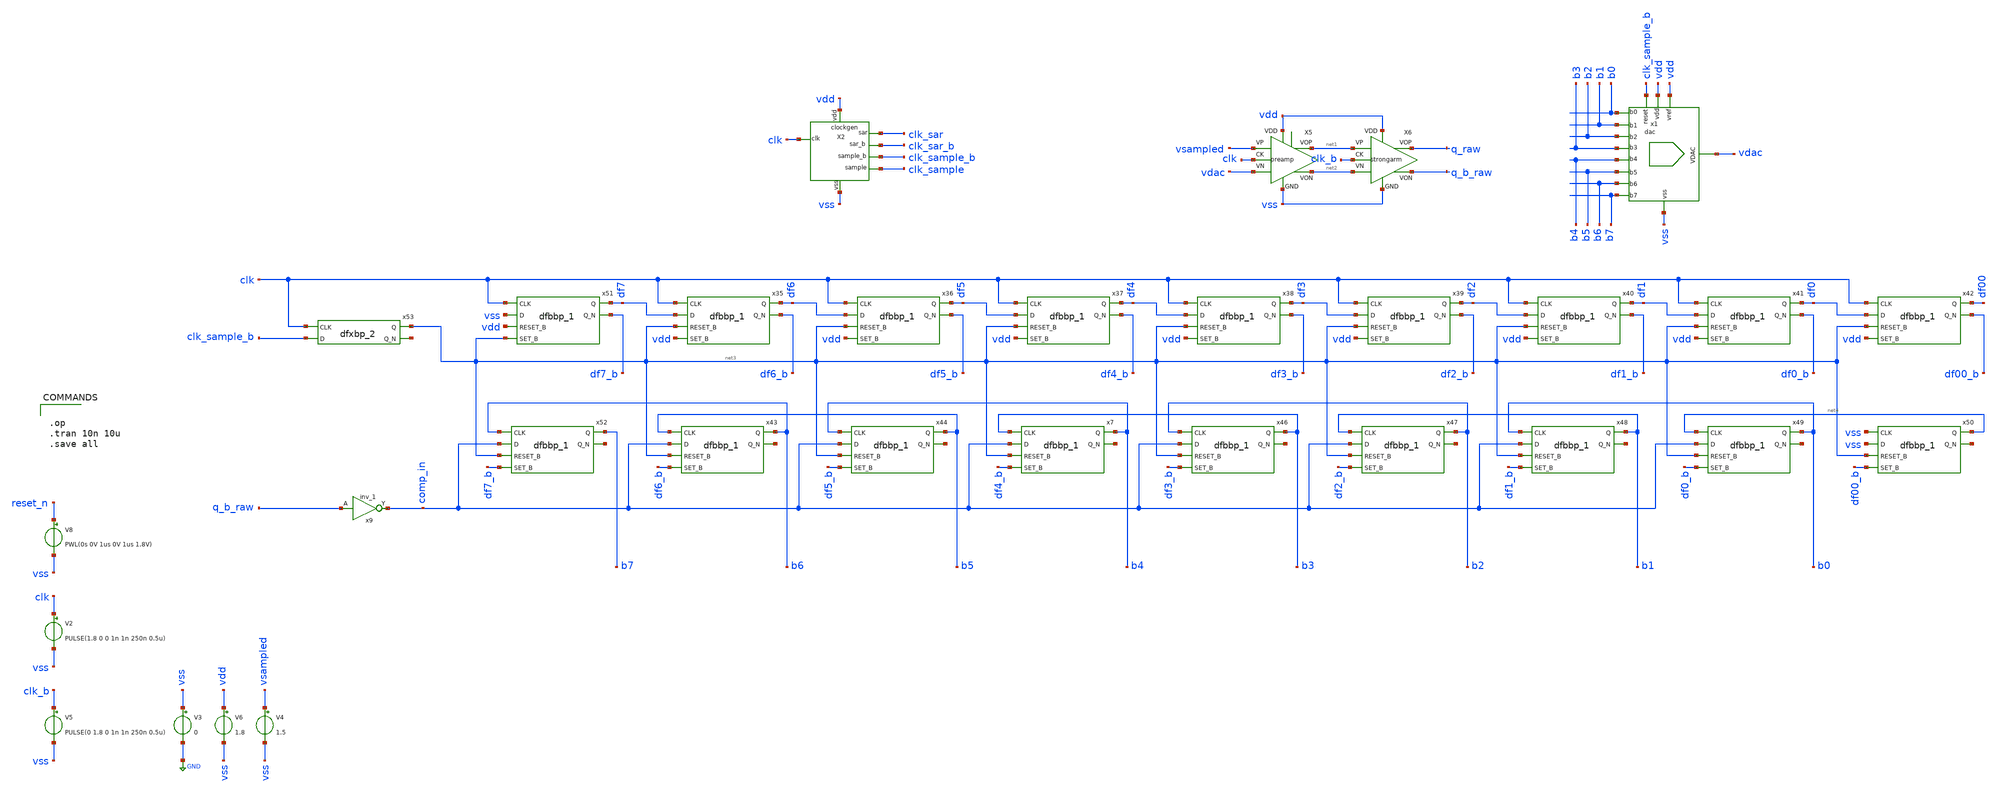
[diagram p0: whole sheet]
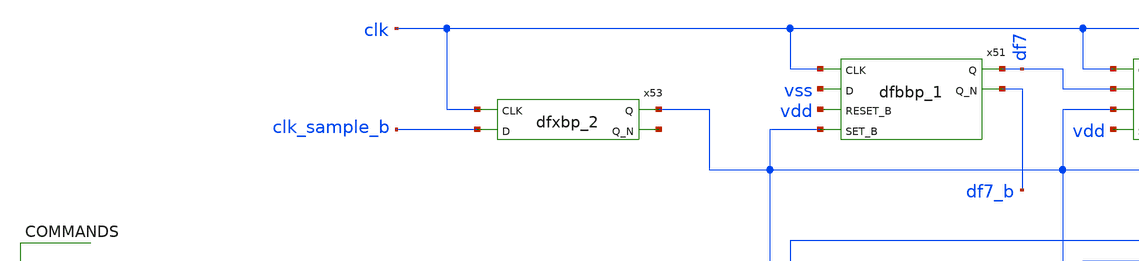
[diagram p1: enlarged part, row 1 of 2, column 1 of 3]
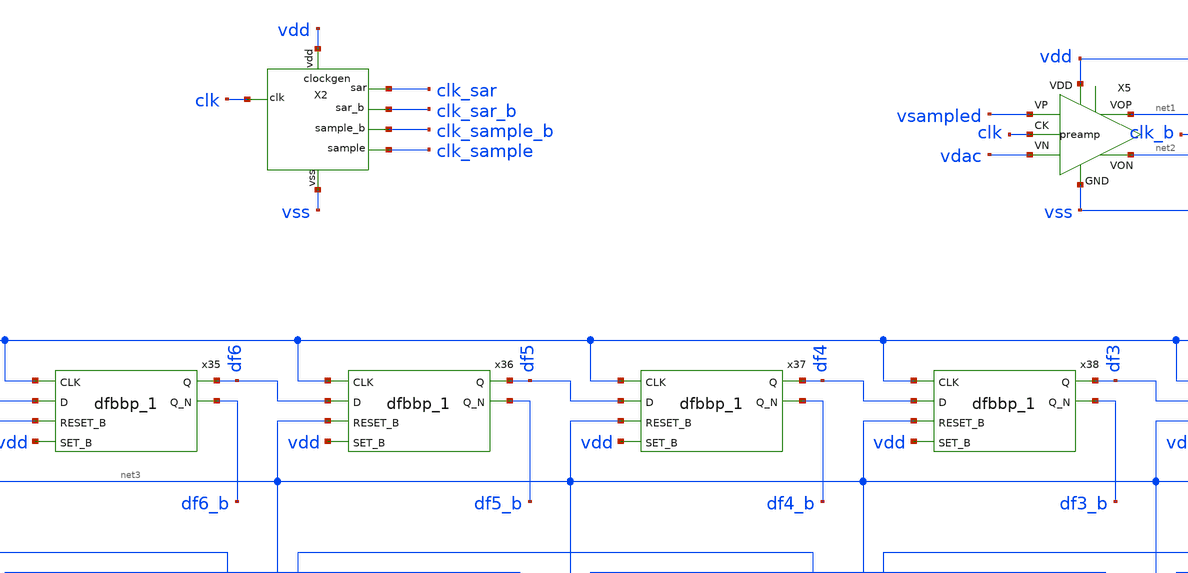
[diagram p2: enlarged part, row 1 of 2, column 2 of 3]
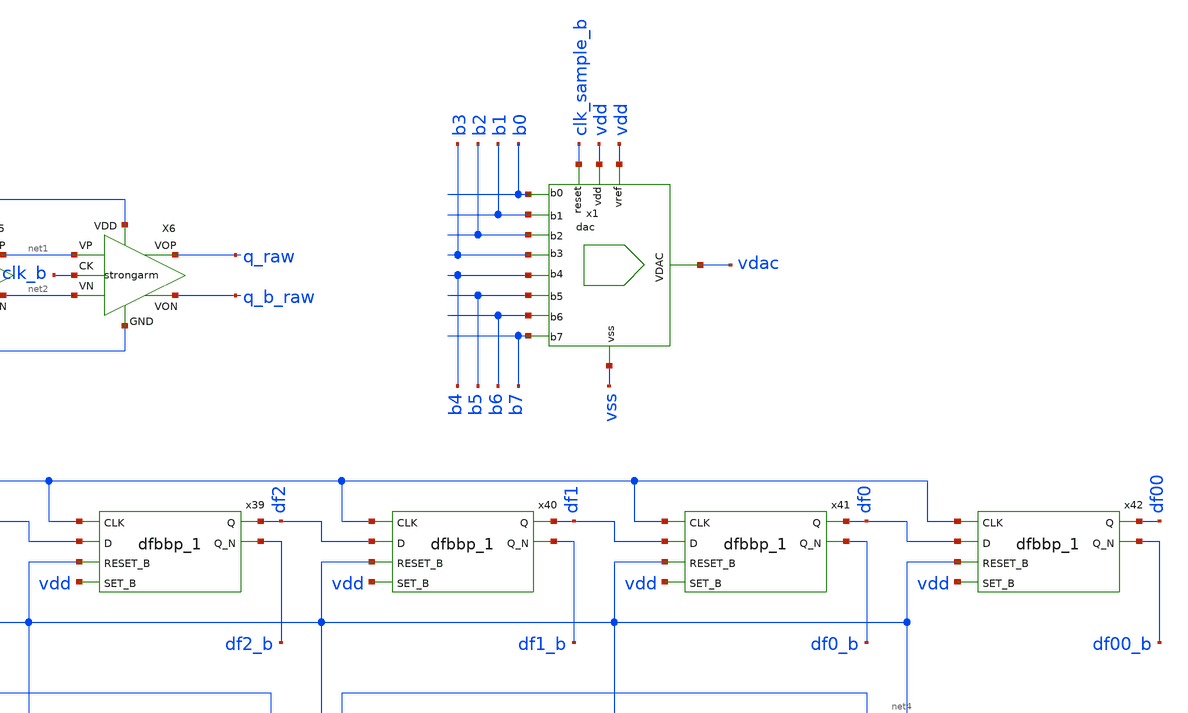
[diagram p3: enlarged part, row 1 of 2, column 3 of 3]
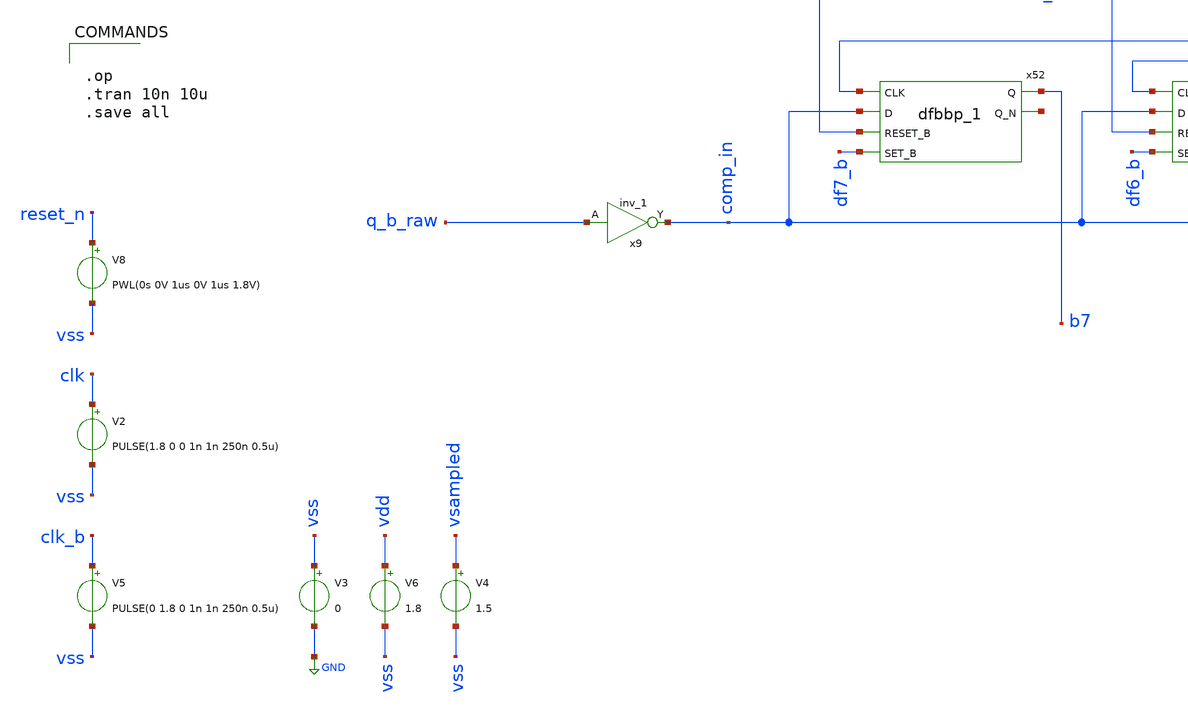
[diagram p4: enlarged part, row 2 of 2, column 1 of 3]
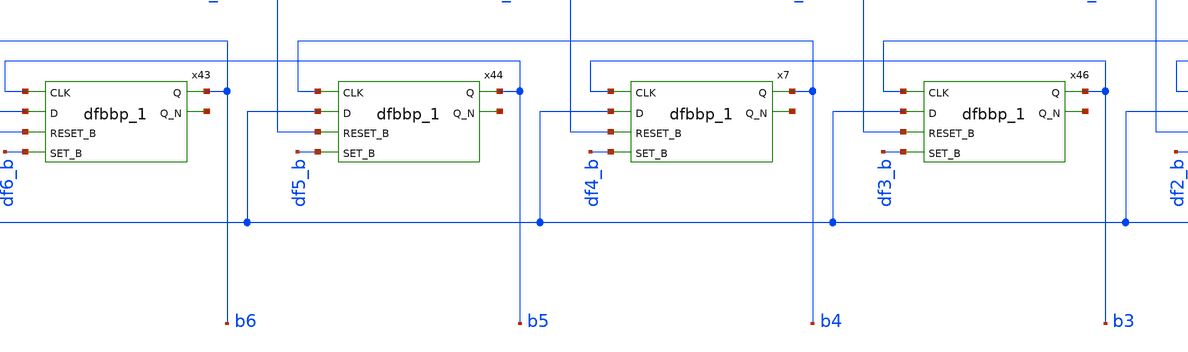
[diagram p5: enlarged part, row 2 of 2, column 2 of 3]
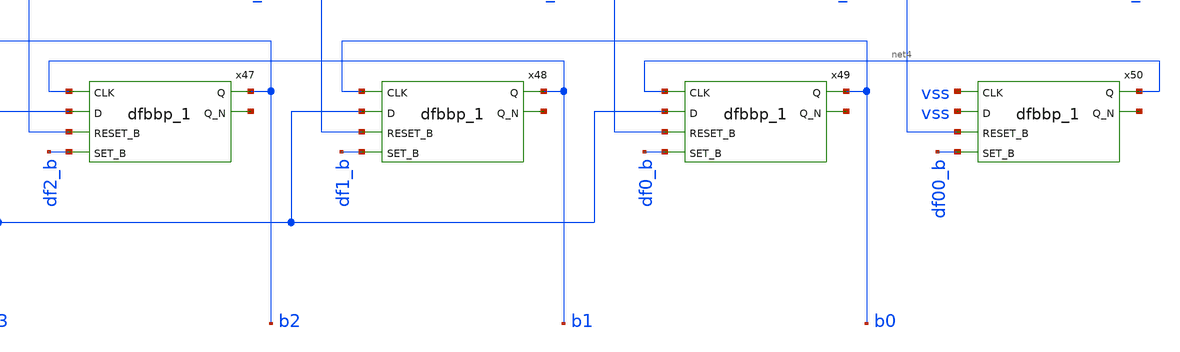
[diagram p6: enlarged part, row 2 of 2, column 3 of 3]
** sch_path: xschem/sar_logic/sar_logic_tb.sch
.lib $::SKYWATER_MODELS/sky130.lib.spice tt
.include $::SKYWATER_STDCELLS/sky130_fd_sc_hd.spice

**.subckt sar_logic_tb
V2 clk vss PULSE(1.8 0 0 1n 1n 250n 0.5u)
V6 vdd vss 1.8
V8 reset_n vss PWL(0s 0V 1us 0V 1us 1.8V)
x1 vss vdac vdd vdd b0 b1 b2 b3 b4 b5 b6 b7 clk_sample_b dac
V3 vss GND 0
V5 clk_b vss PULSE(0 1.8 0 1n 1n 250n 0.5u)
V4 vsampled vss 1.5
X5 vsampled vdac vss net2 net1 vdd clk preamp
X6 net1 net2 vss q_b_raw q_raw vdd clk_b strongarm
x35 clk df7 net3 vdd vss vss vdd vdd df6 df6_b sky130_fd_sc_hd__dfbbp_1
x36 clk df6 net3 vdd vss vss vdd vdd df5 df5_b sky130_fd_sc_hd__dfbbp_1
x37 clk df5 net3 vdd vss vss vdd vdd df4 df4_b sky130_fd_sc_hd__dfbbp_1
x38 clk df4 net3 vdd vss vss vdd vdd df3 df3_b sky130_fd_sc_hd__dfbbp_1
x39 clk df3 net3 vdd vss vss vdd vdd df2 df2_b sky130_fd_sc_hd__dfbbp_1
x40 clk df2 net3 vdd vss vss vdd vdd df1 df1_b sky130_fd_sc_hd__dfbbp_1
x41 clk df1 net3 vdd vss vss vdd vdd df0 df0_b sky130_fd_sc_hd__dfbbp_1
x42 clk df0 net3 vdd vss vss vdd vdd df00 df00_b sky130_fd_sc_hd__dfbbp_1
x43 b5 comp_in net3 df6_b vss vss vdd vdd b6 net5 sky130_fd_sc_hd__dfbbp_1
x44 b4 comp_in net3 df5_b vss vss vdd vdd b5 net6 sky130_fd_sc_hd__dfbbp_1
x7 b3 comp_in net3 df4_b vss vss vdd vdd b4 net7 sky130_fd_sc_hd__dfbbp_1
x46 b2 comp_in net3 df3_b vss vss vdd vdd b3 net8 sky130_fd_sc_hd__dfbbp_1
x47 b1 comp_in net3 df2_b vss vss vdd vdd b2 net9 sky130_fd_sc_hd__dfbbp_1
x48 b0 comp_in net3 df1_b vss vss vdd vdd b1 net10 sky130_fd_sc_hd__dfbbp_1
x49 net4 comp_in net3 df0_b vss vss vdd vdd b0 net11 sky130_fd_sc_hd__dfbbp_1
x50 vss vss net3 df00_b vss vss vdd vdd net4 net12 sky130_fd_sc_hd__dfbbp_1
x51 clk vss vdd net3 vss vss vdd vdd df7 df7_b sky130_fd_sc_hd__dfbbp_1
x52 b6 comp_in net3 df7_b vss vss vdd vdd b7 net13 sky130_fd_sc_hd__dfbbp_1
x53 clk clk_sample_b vss vss vdd vdd net3 net14 sky130_fd_sc_hd__dfxbp_2
x9 q_b_raw vss vss vdd vdd comp_in sky130_fd_sc_hd__inv_1
X2 clk vdd clk_sar clk_sample vss clk_sar_b clk_sample_b clockgen
**** begin user architecture code


.op
.tran 10n 10u
.save all


**** end user architecture code
**.ends

* expanding   symbol:  xschem/dac/dac.sym # of pins=13
** sym_path: xschem/dac/dac.sym
** sch_path: xschem/dac/dac.sch
.subckt dac vss vdac vdd vref s0 s1 s2 s3 s4 s5 s6 s7 reset
*.ipin s7
*.ipin s6
*.ipin s5
*.ipin s4
*.ipin s3
*.ipin s2
*.ipin s1
*.ipin s0
*.iopin vdd
*.iopin vss
*.iopin vref
*.opin vdac
*.ipin reset
XC2 net1 net2 sky130_fd_pr__cap_mim_m3_1 W=w L=l MF=8 m=8
X2 net2 vref vss vdd net14 vss dac_sw
XC1 net1 net3 sky130_fd_pr__cap_mim_m3_1 W=w L=l MF=4 m=4
X3 net3 vref vss vdd net15 vss dac_sw
X4 net4 vref vss vdd net16 vss dac_sw
X5 net5 vref vss vdd net17 vss dac_sw
XC3 net1 net4 sky130_fd_pr__cap_mim_m3_1 W=w L=l MF=2 m=2
XC4 net1 net5 sky130_fd_pr__cap_mim_m3_1 W=w L=l MF=1 m=1
XC5 vss net1 sky130_fd_pr__cap_mim_m3_1 W=w L=l MF=1 m=1
XC6 vdac net6 sky130_fd_pr__cap_mim_m3_1 W=w L=l MF=1 m=1
X1 net6 vref vss vdd net13 vss dac_sw
XC7 vdac net7 sky130_fd_pr__cap_mim_m3_1 W=w L=l MF=2 m=2
X6 net7 vref vss vdd net12 vss dac_sw
XC8 vdac net8 sky130_fd_pr__cap_mim_m3_1 W=w L=l MF=4 m=4
X7 net8 vref vss vdd net11 vss dac_sw
XC9 vdac net9 sky130_fd_pr__cap_mim_m3_1 W=w L=l MF=8 m=8
X8 net9 vref vss vdd net10 vss dac_sw
x9 vss s7 reset vss vss vdd vdd net10 sky130_fd_sc_hd__mux2_1
x10 vss s6 reset vss vss vdd vdd net11 sky130_fd_sc_hd__mux2_1
x11 vss s5 reset vss vss vdd vdd net12 sky130_fd_sc_hd__mux2_1
x12 vss s4 reset vss vss vdd vdd net13 sky130_fd_sc_hd__mux2_1
x13 vss s3 reset vss vss vdd vdd net14 sky130_fd_sc_hd__mux2_1
x14 vss s2 reset vss vss vdd vdd net15 sky130_fd_sc_hd__mux2_1
x15 vss s1 reset vss vss vdd vdd net16 sky130_fd_sc_hd__mux2_1
x16 vss s0 reset vss vss vdd vdd net17 sky130_fd_sc_hd__mux2_1
XM1 vdac net18 vss vss sky130_fd_pr__nfet_01v8 L=0.15 W=1 nf=1 ad='int((nf+1)/2) * W/nf * 0.29' as='int((nf+2)/2) * W/nf * 0.29'
+ pd='2*int((nf+1)/2) * (W/nf + 0.29)' ps='2*int((nf+2)/2) * (W/nf + 0.29)' nrd='0.29 / W' nrs='0.29 / W'
+ sa=0 sb=0 sd=0 mult=1 m=1
x17 reset vss vss vdd vdd net18 sky130_fd_sc_hd__inv_1
XM2 net1 net19 vss vss sky130_fd_pr__nfet_01v8 L=0.15 W=1 nf=1 ad='int((nf+1)/2) * W/nf * 0.29' as='int((nf+2)/2) * W/nf * 0.29'
+ pd='2*int((nf+1)/2) * (W/nf + 0.29)' ps='2*int((nf+2)/2) * (W/nf + 0.29)' nrd='0.29 / W' nrs='0.29 / W'
+ sa=0 sb=0 sd=0 mult=1 m=1
x18 reset vss vss vdd vdd net19 sky130_fd_sc_hd__inv_1
XC10 net1 vdac sky130_fd_pr__cap_mim_m3_1 W=w L=l MF=8/7 m=8/7
.ends


* expanding   symbol:  xschem/comparator/preamp.sym # of pins=7
** sym_path: xschem/comparator/preamp.sym
** sch_path: xschem/comparator/preamp.sch
.subckt preamp VP VN GND VON VOP VDD CK
*.iopin VDD
*.iopin GND
*.iopin CK
*.iopin VON
*.iopin VOP
*.iopin VP
*.iopin VN
XM5 VON VP net1 GND sky130_fd_pr__nfet_01v8 L=1.5 W=2 nf=2 ad='int((2 + 1)/2) * 2 / 2 * 0.29' as='int((2 + 2)/2) * 2 / 2 * 0.29'
+ pd='2*int((2 + 1)/2) * (2 / 2 + 0.29)' ps='2*int((2 + 2)/2) * (2 / 2 + 0.29)' nrd='0.29 / 2 ' nrs='0.29 / 2 '
+ sa=0 sb=0 sd=0 mult=1 m=1
XM6 VON VON VDD VDD sky130_fd_pr__pfet_01v8 L=1.5 W=4 nf=1 ad='int((nf+1)/2) * W/nf * 0.29' as='int((nf+2)/2) * W/nf * 0.29'
+ pd='2*int((nf+1)/2) * (W/nf + 0.29)' ps='2*int((nf+2)/2) * (W/nf + 0.29)' nrd='0.29 / W' nrs='0.29 / W'
+ sa=0 sb=0 sd=0 mult=1 m=1
XM7 VOP VOP VDD VDD sky130_fd_pr__pfet_01v8 L=1.5 W=4 nf=1 ad='int((nf+1)/2) * W/nf * 0.29' as='int((nf+2)/2) * W/nf * 0.29'
+ pd='2*int((nf+1)/2) * (W/nf + 0.29)' ps='2*int((nf+2)/2) * (W/nf + 0.29)' nrd='0.29 / W' nrs='0.29 / W'
+ sa=0 sb=0 sd=0 mult=1 m=1
XM8 VOP VN net1 GND sky130_fd_pr__nfet_01v8 L=1.5 W=2 nf=2 ad='int((2 + 1)/2) * 2 / 2 * 0.29' as='int((2 + 2)/2) * 2 / 2 * 0.29'
+ pd='2*int((2 + 1)/2) * (2 / 2 + 0.29)' ps='2*int((2 + 2)/2) * (2 / 2 + 0.29)' nrd='0.29 / 2 ' nrs='0.29 / 2 '
+ sa=0 sb=0 sd=0 mult=1 m=1
XM9 net1 CK GND GND sky130_fd_pr__nfet_01v8 L=1 W=4 nf=1 ad='int((1 + 1)/2) * 4 / 1 * 0.29' as='int((1 + 2)/2) * 4 / 1 * 0.29'
+ pd='2*int((1 + 1)/2) * (4 / 1 + 0.29)' ps='2*int((1 + 2)/2) * (4 / 1 + 0.29)' nrd='0.29 / 4 ' nrs='0.29 / 4 '
+ sa=0 sb=0 sd=0 mult=1 m=1
.ends


* expanding   symbol:  xschem/comparator/strongarm.sym # of pins=7
** sym_path: xschem/comparator/strongarm.sym
** sch_path: xschem/comparator/strongarm.sch
.subckt strongarm VP VN GND VON VOP VDD CK
*.iopin GND
*.ipin VP
*.opin VOP
*.opin VON
*.ipin VN
*.iopin VDD
*.ipin CK
XM2 net2 CK GND GND sky130_fd_pr__nfet_01v8 L=0.15 W=2 nf=2 ad='int((nf+1)/2) * W/nf * 0.29' as='int((nf+2)/2) * W/nf * 0.29'
+ pd='2*int((nf+1)/2) * (W/nf + 0.29)' ps='2*int((nf+2)/2) * (W/nf + 0.29)' nrd='0.29 / W' nrs='0.29 / W'
+ sa=0 sb=0 sd=0 mult=1 m=1
XM4 VON CK VDD VDD sky130_fd_pr__pfet_01v8 L=0.15 W=1 nf=1 ad='int((nf+1)/2) * W/nf * 0.29' as='int((nf+2)/2) * W/nf * 0.29'
+ pd='2*int((nf+1)/2) * (W/nf + 0.29)' ps='2*int((nf+2)/2) * (W/nf + 0.29)' nrd='0.29 / W' nrs='0.29 / W'
+ sa=0 sb=0 sd=0 mult=1 m=1
XM5 net1 CK VDD VDD sky130_fd_pr__pfet_01v8 L=0.15 W=1 nf=1 ad='int((nf+1)/2) * W/nf * 0.29' as='int((nf+2)/2) * W/nf * 0.29'
+ pd='2*int((nf+1)/2) * (W/nf + 0.29)' ps='2*int((nf+2)/2) * (W/nf + 0.29)' nrd='0.29 / W' nrs='0.29 / W'
+ sa=0 sb=0 sd=0 mult=1 m=1
XM8 net1 VP net2 GND sky130_fd_pr__nfet_01v8 L=0.15 W=2.5 nf=4 ad='int((nf+1)/2) * W/nf * 0.29' as='int((nf+2)/2) * W/nf * 0.29'
+ pd='2*int((nf+1)/2) * (W/nf + 0.29)' ps='2*int((nf+2)/2) * (W/nf + 0.29)' nrd='0.29 / W' nrs='0.29 / W'
+ sa=0 sb=0 sd=0 mult=1 m=1
XM9 VON VOP net1 GND sky130_fd_pr__nfet_01v8 L=0.15 W=2.5 nf=4 ad='int((nf+1)/2) * W/nf * 0.29' as='int((nf+2)/2) * W/nf * 0.29'
+ pd='2*int((nf+1)/2) * (W/nf + 0.29)' ps='2*int((nf+2)/2) * (W/nf + 0.29)' nrd='0.29 / W' nrs='0.29 / W'
+ sa=0 sb=0 sd=0 mult=1 m=1
XM11 VOP CK VDD VDD sky130_fd_pr__pfet_01v8 L=0.15 W=1 nf=1 ad='int((nf+1)/2) * W/nf * 0.29' as='int((nf+2)/2) * W/nf * 0.29'
+ pd='2*int((nf+1)/2) * (W/nf + 0.29)' ps='2*int((nf+2)/2) * (W/nf + 0.29)' nrd='0.29 / W' nrs='0.29 / W'
+ sa=0 sb=0 sd=0 mult=1 m=1
XM12 net3 CK VDD VDD sky130_fd_pr__pfet_01v8 L=0.15 W=1 nf=1 ad='int((nf+1)/2) * W/nf * 0.29' as='int((nf+2)/2) * W/nf * 0.29'
+ pd='2*int((nf+1)/2) * (W/nf + 0.29)' ps='2*int((nf+2)/2) * (W/nf + 0.29)' nrd='0.29 / W' nrs='0.29 / W'
+ sa=0 sb=0 sd=0 mult=1 m=1
XM13 net3 VN net2 GND sky130_fd_pr__nfet_01v8 L=0.15 W=2.5 nf=4 ad='int((nf+1)/2) * W/nf * 0.29' as='int((nf+2)/2) * W/nf * 0.29'
+ pd='2*int((nf+1)/2) * (W/nf + 0.29)' ps='2*int((nf+2)/2) * (W/nf + 0.29)' nrd='0.29 / W' nrs='0.29 / W'
+ sa=0 sb=0 sd=0 mult=1 m=1
XM14 VOP VON net3 GND sky130_fd_pr__nfet_01v8 L=0.15 W=10 nf=1 ad='int((nf+1)/2) * W/nf * 0.29' as='int((nf+2)/2) * W/nf * 0.29'
+ pd='2*int((nf+1)/2) * (W/nf + 0.29)' ps='2*int((nf+2)/2) * (W/nf + 0.29)' nrd='0.29 / W' nrs='0.29 / W'
+ sa=0 sb=0 sd=0 mult=1 m=1
XM15 VOP VON VDD VDD sky130_fd_pr__pfet_01v8 L=0.15 W=2.5 nf=1 ad='int((nf+1)/2) * W/nf * 0.29' as='int((nf+2)/2) * W/nf * 0.29'
+ pd='2*int((nf+1)/2) * (W/nf + 0.29)' ps='2*int((nf+2)/2) * (W/nf + 0.29)' nrd='0.29 / W' nrs='0.29 / W'
+ sa=0 sb=0 sd=0 mult=1 m=1
XM10 VON VOP VDD VDD sky130_fd_pr__pfet_01v8 L=0.15 W=2.5 nf=1 ad='int((nf+1)/2) * W/nf * 0.29' as='int((nf+2)/2) * W/nf * 0.29'
+ pd='2*int((nf+1)/2) * (W/nf + 0.29)' ps='2*int((nf+2)/2) * (W/nf + 0.29)' nrd='0.29 / W' nrs='0.29 / W'
+ sa=0 sb=0 sd=0 mult=1 m=1
.ends


* expanding   symbol:  xschem/clockgen/clockgen.sym # of pins=7
** sym_path: xschem/clockgen/clockgen.sym
** sch_path: xschem/clockgen/clockgen.sch
.subckt clockgen clk vdd clk_sar clk_sample vss clk_sar_b clk_sample_b
*.opin clk_sar
*.opin clk_sample
*.ipin clk
*.iopin vss
*.iopin vdd
*.opin clk_sar_b
*.opin clk_sample_b
x1 clk vss clk_sample vss vss vdd vdd clk_sar sky130_fd_sc_hd__mux2_1
x8 net2 d1 net1 d3 vss vss vdd vdd clk_sample sky130_fd_sc_hd__and4_2
x14 clk net3 rst vss vss vdd vdd d0 net3 sky130_fd_sc_hd__dfrbp_2
x15 d1 d0 vss vss vdd vdd net4 sky130_fd_sc_hd__xor2_1
x16 clk net4 rst vss vss vdd vdd d1 net10 sky130_fd_sc_hd__dfrbp_2
x17 d1 d0 vss vss vdd vdd net7 sky130_fd_sc_hd__and2_1
x18 d2 net7 vss vss vdd vdd net5 sky130_fd_sc_hd__xor2_1
x20 d2 net7 vss vss vdd vdd net11 sky130_fd_sc_hd__and2_1
x21 d3 net11 vss vss vdd vdd net6 sky130_fd_sc_hd__xor2_1
x19 clk net5 rst vss vss vdd vdd d2 net12 sky130_fd_sc_hd__dfrbp_2
x22 clk net6 rst vss vss vdd vdd d3 net13 sky130_fd_sc_hd__dfrbp_2
x23 d0 vss vss vdd vdd net2 sky130_fd_sc_hd__inv_1
x25 d2 vss vss vdd vdd net1 sky130_fd_sc_hd__inv_1
x24 d1 d3 vss vss vdd vdd net9 sky130_fd_sc_hd__and2_1
x26 net9 vss vss vdd vdd net8 sky130_fd_sc_hd__inv_1
x27 clk net8 vss vss vdd vdd rst net14 sky130_fd_sc_hd__dfxbp_2
x2 clk_sar vss vss vdd vdd clk_sar_b sky130_fd_sc_hd__inv_1
x3 clk_sample vss vss vdd vdd clk_sample_b sky130_fd_sc_hd__inv_1
.ends


* expanding   symbol:  xschem/dac/dac_sw.sym # of pins=6
** sym_path: xschem/dac/dac_sw.sym
** sch_path: xschem/dac/dac_sw.sch
.subckt dac_sw c b vss vdd clk a
*.iopin vdd
*.iopin vss
*.ipin clk
*.iopin c
*.iopin a
*.iopin b
XM2 c clk b vss sky130_fd_pr__nfet_01v8 L=0.15 W=5 nf=1 ad='int((nf+1)/2) * W/nf * 0.29' as='int((nf+2)/2) * W/nf * 0.29'
+ pd='2*int((nf+1)/2) * (W/nf + 0.29)' ps='2*int((nf+2)/2) * (W/nf + 0.29)' nrd='0.29 / W' nrs='0.29 / W'
+ sa=0 sb=0 sd=0 mult=1 m=1
XM5 b net1 c vdd sky130_fd_pr__pfet_01v8 L=0.15 W=10 nf=1 ad='int((nf+1)/2) * W/nf * 0.29' as='int((nf+2)/2) * W/nf * 0.29'
+ pd='2*int((nf+1)/2) * (W/nf + 0.29)' ps='2*int((nf+2)/2) * (W/nf + 0.29)' nrd='0.29 / W' nrs='0.29 / W'
+ sa=0 sb=0 sd=0 mult=1 m=1
XM6 c net1 a vss sky130_fd_pr__nfet_01v8 L=0.15 W=5 nf=1 ad='int((nf+1)/2) * W/nf * 0.29' as='int((nf+2)/2) * W/nf * 0.29'
+ pd='2*int((nf+1)/2) * (W/nf + 0.29)' ps='2*int((nf+2)/2) * (W/nf + 0.29)' nrd='0.29 / W' nrs='0.29 / W'
+ sa=0 sb=0 sd=0 mult=1 m=1
XM7 a clk c vdd sky130_fd_pr__pfet_01v8 L=0.15 W=10 nf=1 ad='int((nf+1)/2) * W/nf * 0.29' as='int((nf+2)/2) * W/nf * 0.29'
+ pd='2*int((nf+1)/2) * (W/nf + 0.29)' ps='2*int((nf+2)/2) * (W/nf + 0.29)' nrd='0.29 / W' nrs='0.29 / W'
+ sa=0 sb=0 sd=0 mult=1 m=1
x1 clk vss vss vdd vdd net1 sky130_fd_sc_hd__inv_1
.ends

.GLOBAL GND
.end
